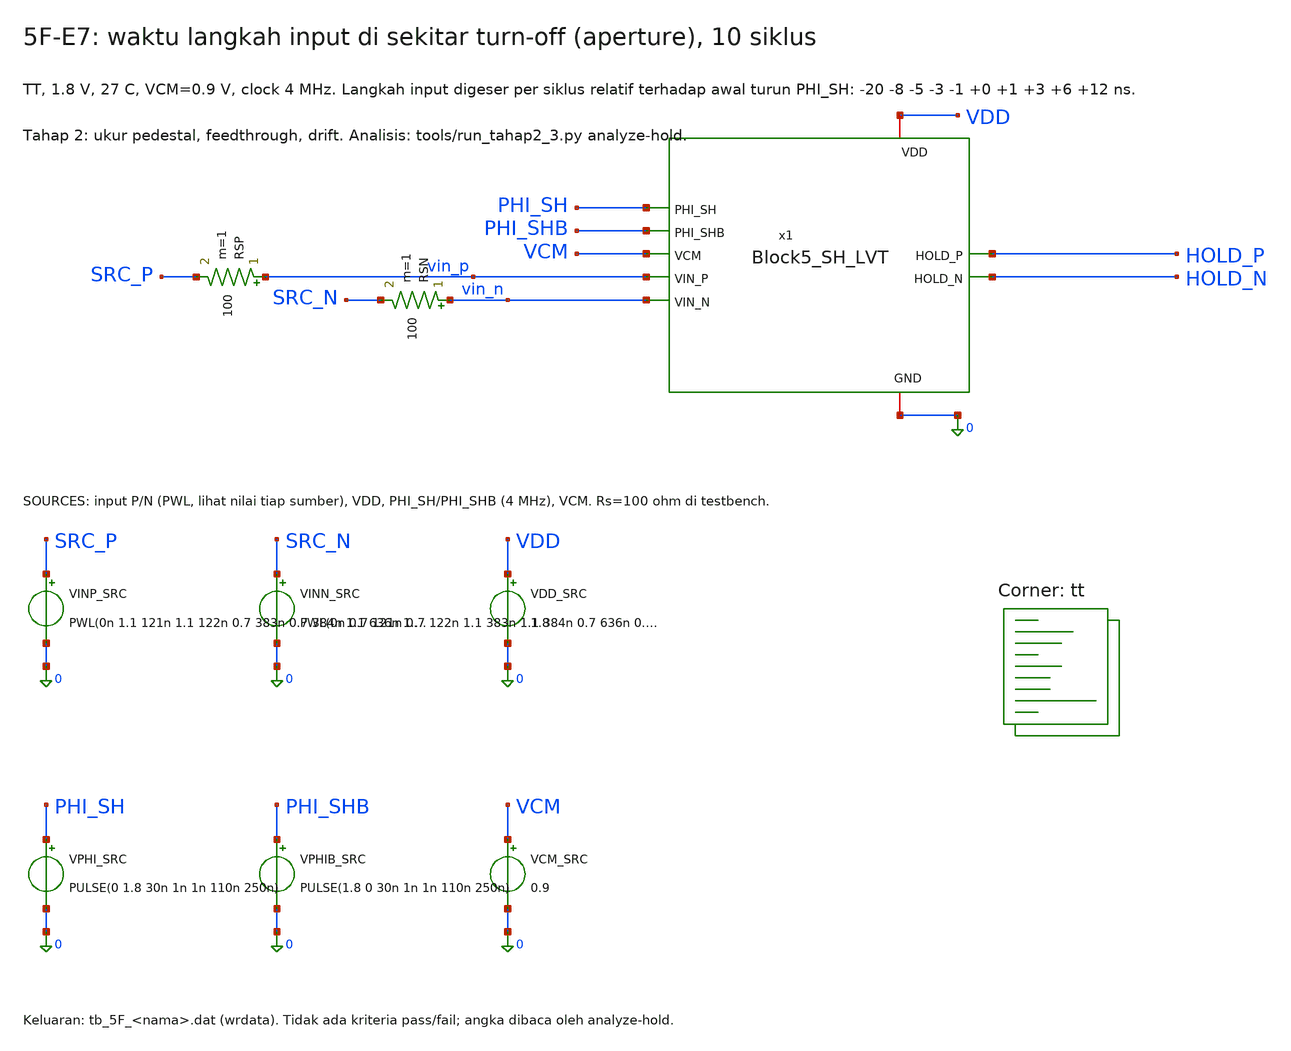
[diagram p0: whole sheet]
** sch_path: blocks/05_Switch_Network/sim/tb_5F_E7_aperture.sch
**.subckt tb_5F_E7_aperture
RSP vin_p SRC_P 100 m=1
RSN vin_n SRC_N 100 m=1
VINP_SRC SRC_P 0 PWL(0n 1.1 121n 1.1 122n 0.7 383n 0.7 384n 1.1 636n 1.1 637n 0.7 888n 0.7 889n 1.1
+ 1140n 1.1 1141n 0.7 1391n 0.7 1392n 1.1 1642n 1.1 1643n 0.7 1894n 0.7 1895n 1.1 2147n 1.1 2148n 0.7 2403n
+ 0.7 2404n 1.1 2700n 1.1)
VINN_SRC SRC_N 0 PWL(0n 0.7 121n 0.7 122n 1.1 383n 1.1 384n 0.7 636n 0.7 637n 1.1 888n 1.1 889n 0.7
+ 1140n 0.7 1141n 1.1 1391n 1.1 1392n 0.7 1642n 0.7 1643n 1.1 1894n 1.1 1895n 0.7 2147n 0.7 2148n 1.1 2403n
+ 1.1 2404n 0.7 2700n 0.7)
VDD_SRC VDD 0 1.8
VPHI_SRC PHI_SH 0 PULSE(0 1.8 30n 1n 1n 110n 250n)
VPHIB_SRC PHI_SHB 0 PULSE(1.8 0 30n 1n 1n 110n 250n)
VCM_SRC VCM 0 0.9
x1 VDD PHI_SH PHI_SHB 0 VCM vin_p HOLD_P HOLD_N vin_n Block5_SH_LVT
**** begin user architecture code
.lib $::SKYWATER_MODELS/sky130.lib.spice tt


* E7_aperture: diagnosa hold error Block 5 (tahap 2). TT, 1.8 V, 27 C.
* .ic hanya kondisi awal numerik, bukan rangkaian reset.
.option scale=1e-6 reltol=1e-5 abstol=1e-15 vntol=1e-8
.temp 27
.ic V(HOLD_P)=0.9 V(HOLD_N)=0.9
.control
save all
set wr_singlescale
set wr_vecnames
set numdgt=15
tran 0.1n 2600n 0 0.1n
wrdata tb_5F_E7_aperture.dat v(SRC_P) v(SRC_N) v(VIN_P) v(VIN_N) v(HOLD_P) v(HOLD_N) v(PHI_SH)
+ v(PHI_SHB)
echo TB_5F_DONE
.endc


**** end user architecture code
**.ends

* expanding   symbol:  blocks/05_Switch_Network/xschem/Block5_SH_LVT.sym # of pins=9
** sym_path: blocks/05_Switch_Network/xschem/Block5_SH_LVT.sym
** sch_path: blocks/05_Switch_Network/xschem/Block5_SH_LVT.sch
.subckt Block5_SH_LVT VDD PHI_SH PHI_SHB GND VCM VIN_P HOLD_P HOLD_N VIN_N
*.ipin VIN_P
*.ipin VIN_N
*.ipin PHI_SH
*.ipin PHI_SHB
*.iopin VDD
*.iopin GND
*.ipin VCM
*.opin HOLD_P
*.opin HOLD_N
CH_P HOLD_P VCM 1p m=1
CH_N HOLD_N VCM 1p m=1
x3 VIN_P HOLD_P PHI_SHB PHI_SH VDD GND TG_SC_LVT
x1 VIN_N HOLD_N PHI_SHB PHI_SH VDD GND TG_SC_LVT
.ends


* expanding   symbol:  blocks/05_Switch_Network/xschem/TG_SC_LVT.sym # of pins=6
** sym_path: blocks/05_Switch_Network/xschem/TG_SC_LVT.sym
** sch_path: blocks/05_Switch_Network/xschem/TG_SC_LVT.sch
.subckt TG_SC_LVT A B CLK_P CLK_N VDD GND
*.iopin A
*.iopin B
*.ipin CLK_P
*.ipin CLK_N
*.iopin VDD
*.iopin GND
XMP A CLK_P B VDD sky130_fd_pr__pfet_01v8_lvt L=0.35 W=8 nf=1 ad='int((1 + 1)/2) * 8 / 1 * 0.29' as='int((1 + 2)/2) * 8 / 1 * 0.29'
+ pd='2*int((1 + 1)/2) * (8 / 1 + 0.29)' ps='2*int((1 + 2)/2) * (8 / 1 + 0.29)' nrd='0.29 / 8 ' nrs='0.29 / 8 '
+ sa=0 sb=0 sd=0 mult=1
XMN A CLK_N B GND sky130_fd_pr__nfet_01v8_lvt L=0.15 W=4 nf=1 ad='int((1 + 1)/2) * 4 / 1 * 0.29' as='int((1 + 2)/2) * 4 / 1 * 0.29'
+ pd='2*int((1 + 1)/2) * (4 / 1 + 0.29)' ps='2*int((1 + 2)/2) * (4 / 1 + 0.29)' nrd='0.29 / 4 ' nrs='0.29 / 4 '
+ sa=0 sb=0 sd=0 mult=1
.ends

.end
